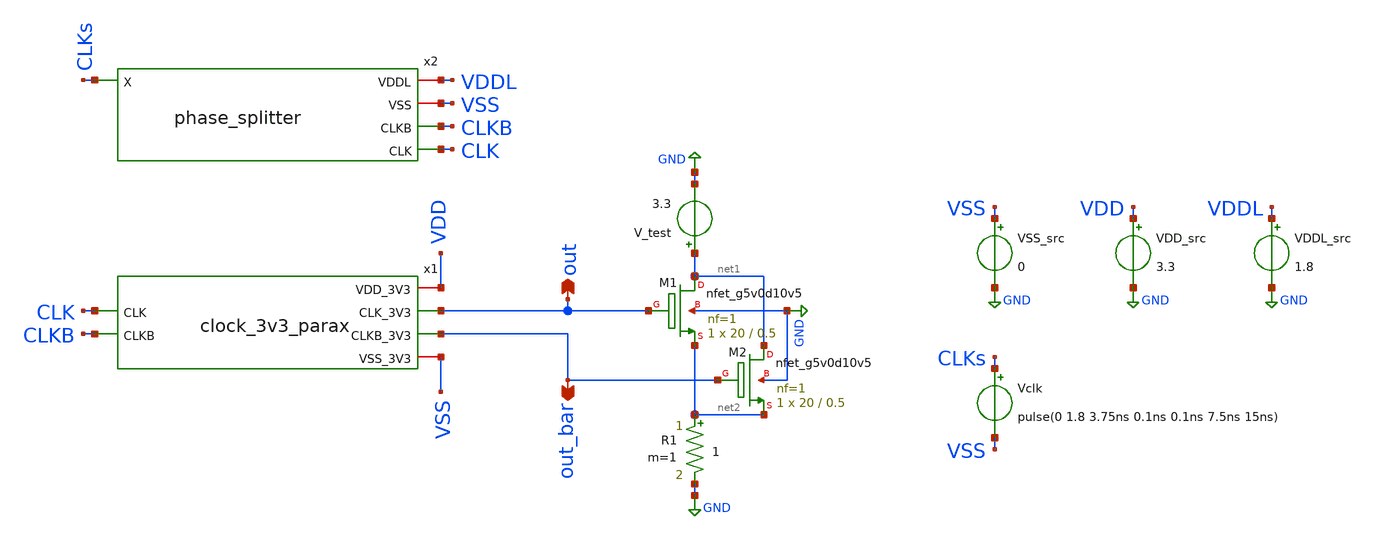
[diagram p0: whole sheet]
** sch_path: xschem/clock_3v3/testbench.sch
**.subckt testbench out out_bar
*.opin out
*.opin out_bar
VDD_src VDD GND 3.3
VSS_src VSS GND 0
XM1 net1 out net2 GND sky130_fd_pr__nfet_g5v0d10v5 L=0.5 W=20 nf=1 ad='int((nf+1)/2) * W/nf * 0.29' as='int((nf+2)/2) * W/nf * 0.29'
+ pd='2*int((nf+1)/2) * (W/nf + 0.29)' ps='2*int((nf+2)/2) * (W/nf + 0.29)' nrd='0.29 / W' nrs='0.29 / W'
+ sa=0 sb=0 sd=0 mult=1 m=1
R1 net2 GND 1 m=1
Vclk CLKs VSS pulse(0 1.8 3.75ns 0.1ns 0.1ns 7.5ns 15ns)
V_test net1 GND 3.3
x1 out CLK VSS VDD CLKB out_bar clock_3v3_parax
XM2 net1 out_bar net2 GND sky130_fd_pr__nfet_g5v0d10v5 L=0.5 W=20 nf=1 ad='int((nf+1)/2) * W/nf * 0.29'
+ as='int((nf+2)/2) * W/nf * 0.29' pd='2*int((nf+1)/2) * (W/nf + 0.29)' ps='2*int((nf+2)/2) * (W/nf + 0.29)'
+ nrd='0.29 / W' nrs='0.29 / W' sa=0 sb=0 sd=0 mult=1 m=1
VDDL_src VDDL GND 1.8
x2 VDDL VSS CLKB CLKs CLK phase_splitter
**** begin user architecture code

** opencircuitdesign pdks install
.lib $::SKYWATER_MODELS/sky130.lib.spice tt_mm
.include /home/ttuser/pdk/sky130A/libs.ref/sky130_fd_sc_hd/spice/sky130_fd_sc_hd.spice
.include /home/ttuser/pdk/sky130A/libs.ref/sky130_fd_sc_hvl/spice/sky130_fd_sc_hvl.spice




  .option savecurrents
  .control
  set numruns = 100
  let run = 0

  setplot new
  set mc_plot = $curplot
  let d10 = unitvec($numruns) - 1
  let d10b = unitvec($numruns) - 1
  let d50 = unitvec($numruns) - 1
  let d50b = unitvec($numruns) - 1
  let dt = unitvec($numruns) - 1
  let dtb = unitvec($numruns) - 1
  let d90 = unitvec($numruns) - 1
  let d90b = unitvec($numruns) - 1
  let i_rms = unitvec($numruns) - 1

  dowhile $&run < $numruns
    reset
    set temp = 27
    tran 0.01n 60n
    remzerovec
    write testbench.raw
    set appendwrite

    meas tran dead_10_on TRIG out_bar val=0.33 FALL=1 TARG out val=0.33 RISE=1
    meas tran dead_10_off TRIG out val=0.33 FALL=1 TARG out_bar val=0.33 RISE=1
    let d10 = min(dead_10_on, dead_10_off)
    let d10b = max(dead_10_on, dead_10_off)
    set d10s = $&d10
    set d10bs = $&d10b

    meas tran dead_50_on TRIG out_bar val=1.65 FALL=1 TARG out val=1.65 RISE=1
    meas tran dead_50_off TRIG out val=1.65 FALL=1 TARG out_bar val=1.65 RISE=1
    let d50 = min(dead_50_on, dead_50_off)
    let d50b = max(dead_50_on, dead_50_off)
    set d50s = $&d50
    set d50bs = $&d50b

    meas tran dead_t_on TRIG out_bar val=2.7 FALL=1 TARG out val=2.7 RISE=1
    meas tran dead_t_off TRIG out val=2.97 FALL=1 TARG out_bar val=2.7 RISE=1
    let dt = min(dead_t_on, dead_t_off)
    let dtb = max(dead_t_on, dead_t_off)
    set dts = $&dt
    set dtbs = $&dtb

    meas tran dead_90_on TRIG out_bar val=2.97 FALL=1 TARG out val=2.97 RISE=1
    meas tran dead_90_off TRIG out val=2.97 FALL=1 TARG out_bar val=2.97 RISE=1
    let d90 = min(dead_90_on, dead_90_off)
    let d90b = max(dead_90_on, dead_90_off)
    set d90s = $&d90
    set d90bs = $&d90b

    let i2 = (abs(vdd_src#branch)+abs(vddl_src#branch))^2
    meas tran ms AVG i2
    let i_rms = sqrt(ms)
    set i_rms_s = $&i_rms

*    let i_scaled = 6000*(abs(vdd_src#branch)+abs(vddl_src#branch))
*    plot clk out out_bar i_scaled xl 3.5n 5.5n

    set tran_plot = $curplot
    setplot $mc_plot
    let d10[$&run] = $d10s
    let d10b[$&run] = $d10bs
    let d50[$&run] = $d50s
    let d50b[$&run] = $d50bs
    let dt[$&run] = $dts
    let dtb[$&run] = $dtbs
    let d90[$&run] = $d90s
    let d90b[$&run] = $d90bs
    let i_rms[$&run] = $i_rms_s
    setplot $tran_plot

    let run = run + 1
  end
  setplot $mc_plot
  let min_d10 = minimum(d10)*1e9
  let max_d10 = maximum(d10b)*1e9
  let min_d50 = minimum(d50)*1e9
  let max_d50 = maximum(d50b)*1e9
  let min_dt = minimum(dt)*1e9
  let max_dt = maximum(dtb)*1e9
  let min_d90 = minimum(d90)*1e9
  let max_d90 = maximum(d90b)*1e9
  let min_i_rms = minimum(i_rms)*1e6
  let max_i_rms = maximum(i_rms)*1e6
  echo ""
  echo "Dead time (10%): $&min_d10 - $&max_d10 ns"
  echo "Dead time (50%): $&min_d50 - $&max_d50 ns"
  echo "Dead time (2V7): $&min_dt - $&max_dt ns"
  echo "Dead time (90%): $&min_d90 - $&max_d90 ns"
  echo "I_rms: $&min_i_rms - $&max_i_rms uA"
  .endc



**** end user architecture code
**.ends

* expanding   symbol:  clock_3v3/clock_3v3_parax.sym # of pins=6
** sym_path: xschem/clock_3v3/clock_3v3.sym
.include [file normalize ../mag/clock_3v3.sim.spice]

* expanding   symbol:  clock_3v3/phase_splitter.sym # of pins=5
** sym_path: xschem/clock_3v3/phase_splitter.sym
** sch_path: xschem/clock_3v3/phase_splitter.sch
.subckt phase_splitter VDDL VSS CLKB X CLK
*.ipin X
*.opin CLK
*.opin CLKB
*.iopin VDDL
*.iopin VSS
x2 net1 VSS VSS VDDL VDDL net2 sky130_fd_sc_hd__clkinv_2
x1 X VSS VSS VDDL VDDL net1 sky130_fd_sc_hd__clkinv_2
x3 net1 VSS VSS VDDL VDDL CLK sky130_fd_sc_hd__clkinv_2
x4 net2 VSS VSS VDDL VDDL CLKB sky130_fd_sc_hd__clkinv_2
.ends

.GLOBAL GND
.end
